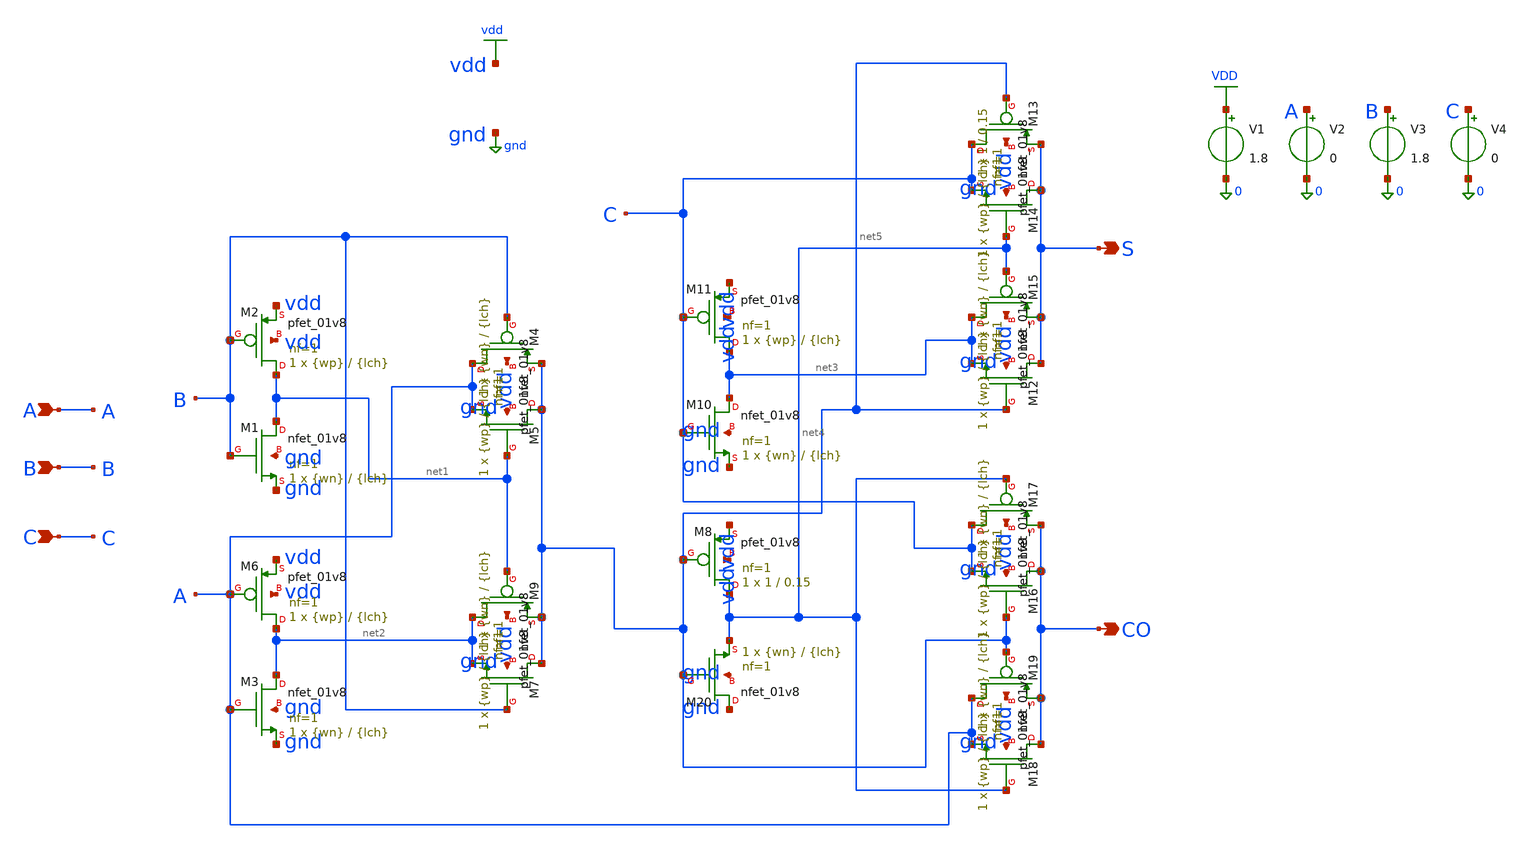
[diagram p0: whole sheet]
** sch_path: tb_WL_FA20T.sch
**.subckt tb_WL_FA20T A B C S CO
*.ipin A
*.ipin B
*.ipin C
*.opin S
*.opin CO
XM1 net1 B gnd gnd sky130_fd_pr__nfet_01v8 L={lch} W={wn} nf=1 ad='int((1 + 1)/2) * {wn} / 1 * 0.29'
+ as='int((1 + 2)/2) * {wn} / 1 * 0.29' pd='2*int((1 + 1)/2) * ({wn} / 1 + 0.29)' ps='2*int((1 + 2)/2) * ({wn} / 1 + 0.29)'
+ nrd='0.29 / {wn} ' nrs='0.29 / {wn} ' sa=0 sb=0 sd=0 mult=1 m=1
XM2 net1 B vdd vdd sky130_fd_pr__pfet_01v8 L={lch} W={wp} nf=1 ad='int((1 + 1)/2) * {wp} / 1 * 0.29'
+ as='int((1 + 2)/2) * {wp} / 1 * 0.29' pd='2*int((1 + 1)/2) * ({wp} / 1 + 0.29)' ps='2*int((1 + 2)/2) * ({wp} / 1 + 0.29)'
+ nrd='0.29 / {wp} ' nrs='0.29 / {wp} ' sa=0 sb=0 sd=0 mult=1 m=1
XM8 net4 net5 vdd vdd sky130_fd_pr__pfet_01v8 L=0.15 W=1 nf=1 ad='int((1 + 1)/2) * 1 / 1 * 0.29' as='int((1 + 2)/2) * 1 / 1 * 0.29'
+ pd='2*int((1 + 1)/2) * (1 / 1 + 0.29)' ps='2*int((1 + 2)/2) * (1 / 1 + 0.29)' nrd='0.29 / 1 ' nrs='0.29 / 1 '
+ sa=0 sb=0 sd=0 mult=1 m=1
XM14 S net4 C gnd sky130_fd_pr__nfet_01v8 L=0.15 W=1 nf=1 ad='int((1 + 1)/2) * 1 / 1 * 0.29' as='int((1 + 2)/2) * 1 / 1 * 0.29'
+ pd='2*int((1 + 1)/2) * (1 / 1 + 0.29)' ps='2*int((1 + 2)/2) * (1 / 1 + 0.29)' nrd='0.29 / 1 ' nrs='0.29 / 1 '
+ sa=0 sb=0 sd=0 mult=1 m=1
V1 VDD 0 1.8
V2 A 0 0
V3 B 0 1.8
V4 C 0 0
XM4 A B net5 vdd sky130_fd_pr__pfet_01v8 L={lch} W={wp} nf=1 ad='int((1 + 1)/2) * {wp} / 1 * 0.29' as='int((1 + 2)/2) * {wp} / 1 * 0.29'
+ pd='2*int((1 + 1)/2) * ({wp} / 1 + 0.29)' ps='2*int((1 + 2)/2) * ({wp} / 1 + 0.29)' nrd='0.29 / {wp} '
+ nrs='0.29 / {wp} ' sa=0 sb=0 sd=0 mult=1 m=1
XM6 net2 A vdd vdd sky130_fd_pr__pfet_01v8 L={lch} W={wp} nf=1 ad='int((1 + 1)/2) * {wp} / 1 * 0.29'
+ as='int((1 + 2)/2) * {wp} / 1 * 0.29' pd='2*int((1 + 1)/2) * ({wp} / 1 + 0.29)' ps='2*int((1 + 2)/2) * ({wp} / 1 + 0.29)'
+ nrd='0.29 / {wp} ' nrs='0.29 / {wp} ' sa=0 sb=0 sd=0 mult=1 m=1
XM9 net2 net1 net5 vdd sky130_fd_pr__pfet_01v8 L={lch} W={wp} nf=1 ad='int((1 + 1)/2) * {wp} / 1 * 0.29'
+ as='int((1 + 2)/2) * {wp} / 1 * 0.29' pd='2*int((1 + 1)/2) * ({wp} / 1 + 0.29)' ps='2*int((1 + 2)/2) * ({wp} / 1 + 0.29)'
+ nrd='0.29 / {wp} ' nrs='0.29 / {wp} ' sa=0 sb=0 sd=0 mult=1 m=1
XM11 net3 C vdd vdd sky130_fd_pr__pfet_01v8 L={lch} W={wp} nf=1 ad='int((1 + 1)/2) * {wp} / 1 * 0.29'
+ as='int((1 + 2)/2) * {wp} / 1 * 0.29' pd='2*int((1 + 1)/2) * ({wp} / 1 + 0.29)' ps='2*int((1 + 2)/2) * ({wp} / 1 + 0.29)'
+ nrd='0.29 / {wp} ' nrs='0.29 / {wp} ' sa=0 sb=0 sd=0 mult=1 m=1
XM13 C net5 S vdd sky130_fd_pr__pfet_01v8 L={lch} W={wp} nf=1 ad='int((1 + 1)/2) * {wp} / 1 * 0.29' as='int((1 + 2)/2) * {wp} / 1 * 0.29'
+ pd='2*int((1 + 1)/2) * ({wp} / 1 + 0.29)' ps='2*int((1 + 2)/2) * ({wp} / 1 + 0.29)' nrd='0.29 / {wp} '
+ nrs='0.29 / {wp} ' sa=0 sb=0 sd=0 mult=1 m=1
XM15 net3 net4 S vdd sky130_fd_pr__pfet_01v8 L={lch} W={wp} nf=1 ad='int((1 + 1)/2) * {wp} / 1 * 0.29'
+ as='int((1 + 2)/2) * {wp} / 1 * 0.29' pd='2*int((1 + 1)/2) * ({wp} / 1 + 0.29)' ps='2*int((1 + 2)/2) * ({wp} / 1 + 0.29)'
+ nrd='0.29 / {wp} ' nrs='0.29 / {wp} ' sa=0 sb=0 sd=0 mult=1 m=1
XM17 C net4 CO vdd sky130_fd_pr__pfet_01v8 L={lch} W={wp} nf=1 ad='int((1 + 1)/2) * {wp} / 1 * 0.29'
+ as='int((1 + 2)/2) * {wp} / 1 * 0.29' pd='2*int((1 + 1)/2) * ({wp} / 1 + 0.29)' ps='2*int((1 + 2)/2) * ({wp} / 1 + 0.29)'
+ nrd='0.29 / {wp} ' nrs='0.29 / {wp} ' sa=0 sb=0 sd=0 mult=1 m=1
XM19 A net5 CO vdd sky130_fd_pr__pfet_01v8 L={lch} W={wp} nf=1 ad='int((1 + 1)/2) * {wp} / 1 * 0.29'
+ as='int((1 + 2)/2) * {wp} / 1 * 0.29' pd='2*int((1 + 1)/2) * ({wp} / 1 + 0.29)' ps='2*int((1 + 2)/2) * ({wp} / 1 + 0.29)'
+ nrd='0.29 / {wp} ' nrs='0.29 / {wp} ' sa=0 sb=0 sd=0 mult=1 m=1
XM3 net2 A gnd gnd sky130_fd_pr__nfet_01v8 L={lch} W={wn} nf=1 ad='int((1 + 1)/2) * {wn} / 1 * 0.29'
+ as='int((1 + 2)/2) * {wn} / 1 * 0.29' pd='2*int((1 + 1)/2) * ({wn} / 1 + 0.29)' ps='2*int((1 + 2)/2) * ({wn} / 1 + 0.29)'
+ nrd='0.29 / {wn} ' nrs='0.29 / {wn} ' sa=0 sb=0 sd=0 mult=1 m=1
XM5 net5 net1 A gnd sky130_fd_pr__nfet_01v8 L={lch} W={wn} nf=1 ad='int((1 + 1)/2) * {wn} / 1 * 0.29'
+ as='int((1 + 2)/2) * {wn} / 1 * 0.29' pd='2*int((1 + 1)/2) * ({wn} / 1 + 0.29)' ps='2*int((1 + 2)/2) * ({wn} / 1 + 0.29)'
+ nrd='0.29 / {wn} ' nrs='0.29 / {wn} ' sa=0 sb=0 sd=0 mult=1 m=1
XM7 net5 B net2 gnd sky130_fd_pr__nfet_01v8 L={lch} W={wn} nf=1 ad='int((1 + 1)/2) * {wn} / 1 * 0.29'
+ as='int((1 + 2)/2) * {wn} / 1 * 0.29' pd='2*int((1 + 1)/2) * ({wn} / 1 + 0.29)' ps='2*int((1 + 2)/2) * ({wn} / 1 + 0.29)'
+ nrd='0.29 / {wn} ' nrs='0.29 / {wn} ' sa=0 sb=0 sd=0 mult=1 m=1
XM12 S net5 net3 gnd sky130_fd_pr__nfet_01v8 L={lch} W={wn} nf=1 ad='int((1 + 1)/2) * {wn} / 1 * 0.29'
+ as='int((1 + 2)/2) * {wn} / 1 * 0.29' pd='2*int((1 + 1)/2) * ({wn} / 1 + 0.29)' ps='2*int((1 + 2)/2) * ({wn} / 1 + 0.29)'
+ nrd='0.29 / {wn} ' nrs='0.29 / {wn} ' sa=0 sb=0 sd=0 mult=1 m=1
XM16 CO net5 C gnd sky130_fd_pr__nfet_01v8 L={lch} W={wn} nf=1 ad='int((1 + 1)/2) * {wn} / 1 * 0.29'
+ as='int((1 + 2)/2) * {wn} / 1 * 0.29' pd='2*int((1 + 1)/2) * ({wn} / 1 + 0.29)' ps='2*int((1 + 2)/2) * ({wn} / 1 + 0.29)'
+ nrd='0.29 / {wn} ' nrs='0.29 / {wn} ' sa=0 sb=0 sd=0 mult=1 m=1
XM18 CO net4 A gnd sky130_fd_pr__nfet_01v8 L={lch} W={wn} nf=1 ad='int((1 + 1)/2) * {wn} / 1 * 0.29'
+ as='int((1 + 2)/2) * {wn} / 1 * 0.29' pd='2*int((1 + 1)/2) * ({wn} / 1 + 0.29)' ps='2*int((1 + 2)/2) * ({wn} / 1 + 0.29)'
+ nrd='0.29 / {wn} ' nrs='0.29 / {wn} ' sa=0 sb=0 sd=0 mult=1 m=1
XM20 gnd net5 net4 gnd sky130_fd_pr__nfet_01v8 L={lch} W={wn} nf=1 ad='int((1 + 1)/2) * {wn} / 1 * 0.29'
+ as='int((1 + 2)/2) * {wn} / 1 * 0.29' pd='2*int((1 + 1)/2) * ({wn} / 1 + 0.29)' ps='2*int((1 + 2)/2) * ({wn} / 1 + 0.29)'
+ nrd='0.29 / {wn} ' nrs='0.29 / {wn} ' sa=0 sb=0 sd=0 mult=1 m=1
XM10 net3 C gnd gnd sky130_fd_pr__nfet_01v8 L={lch} W={wn} nf=1 ad='int((1 + 1)/2) * {wn} / 1 * 0.29'
+ as='int((1 + 2)/2) * {wn} / 1 * 0.29' pd='2*int((1 + 1)/2) * ({wn} / 1 + 0.29)' ps='2*int((1 + 2)/2) * ({wn} / 1 + 0.29)'
+ nrd='0.29 / {wn} ' nrs='0.29 / {wn} ' sa=0 sb=0 sd=0 mult=1 m=1
**** begin user architecture code
.lib /foss/pdks/sky130A/libs.tech/ngspice/sky130.lib.spice tt
.param wp=2 wn=1 lch=0.15
.control
foreach w 1 1.5 2 2.5 3 3.5 4 4.5 5
    alterparam wp = $w
    reset
    dc V2 0 1.8 0.02
    meas dc vm_sum WHEN v(s)=0.9
    meas dc vm_cout WHEN v(co)=0.9

    echo $w $&vm_sum $&vm_cout >> /foss/designs/dc_results_20T.txt
    write /foss/designs/dc_wp_20T{$w}.raw v(a) v(s) v(co)
end
.endc
.end


**** end user architecture code
**.ends
.GLOBAL VDD
.GLOBAL vdd
.GLOBAL gnd
.end
